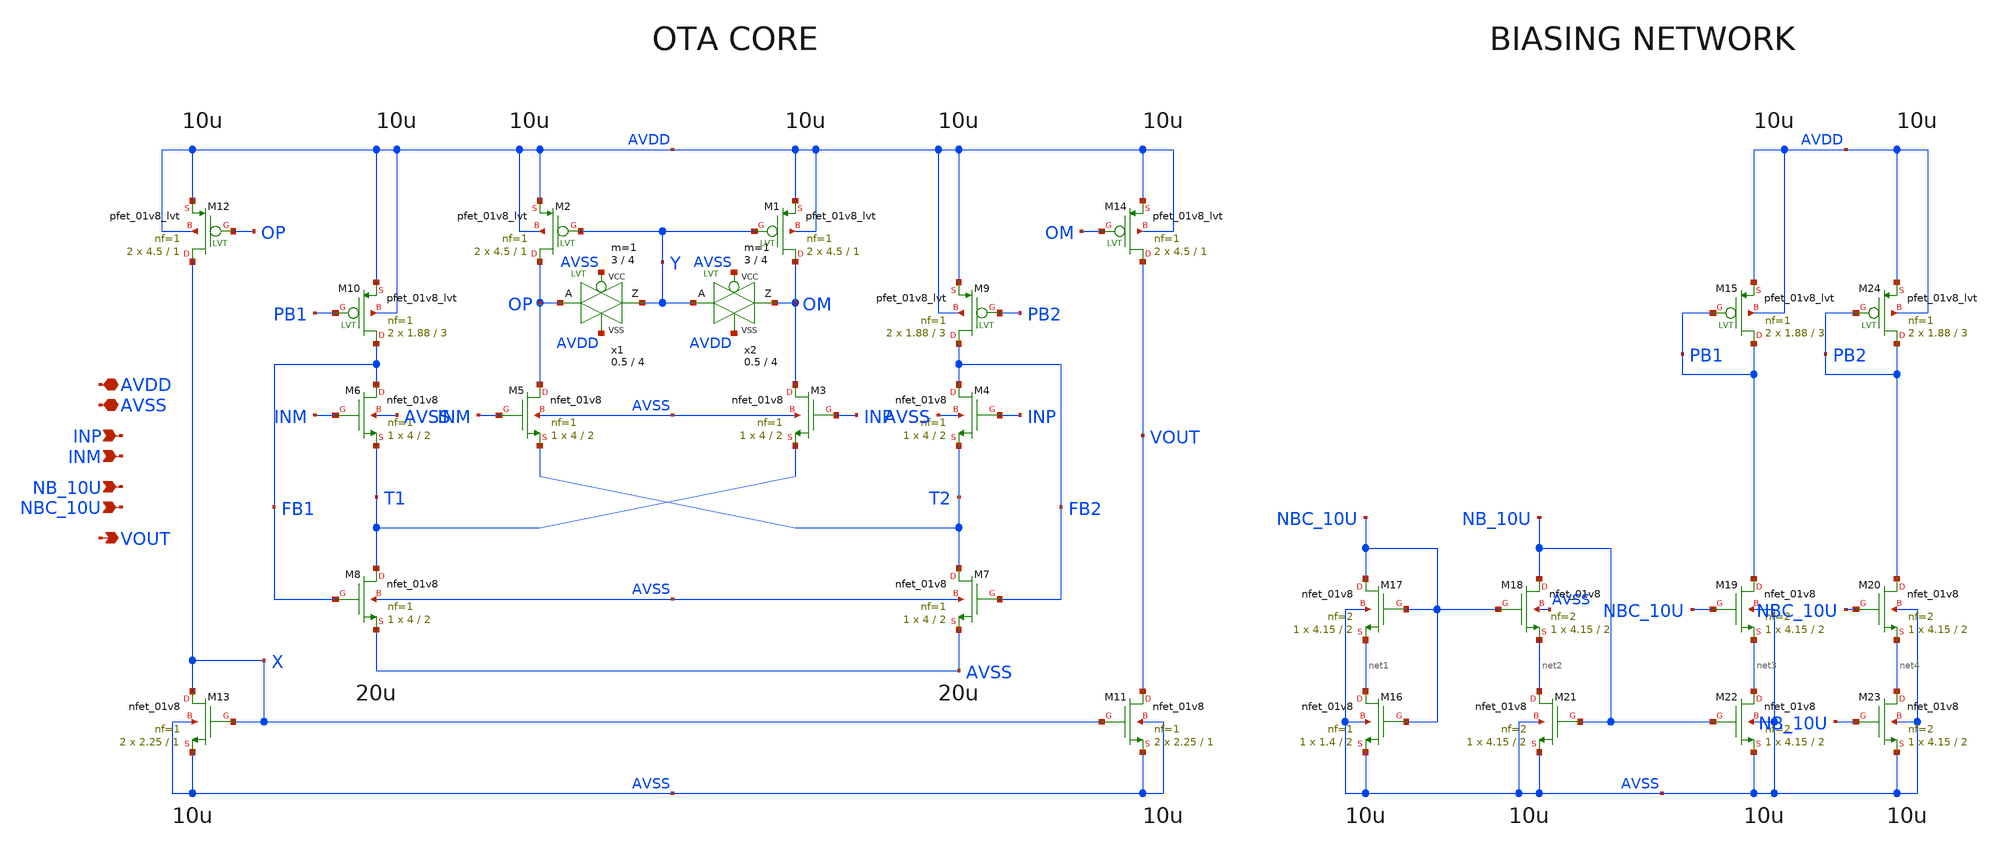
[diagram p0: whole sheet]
** sch_path: ISSCC25/submitted_notebooks/analog_vibes/sim_pex/xschem/ota.sch
**.subckt ota AVDD AVSS INP INM NB_10U NBC_10U VOUT
*.iopin AVDD
*.iopin AVSS
*.ipin INP
*.ipin INM
*.ipin NB_10U
*.ipin NBC_10U
*.opin VOUT
XM1 OM Y AVDD AVDD sky130_fd_pr__pfet_01v8_lvt L=1 W=4.5 nf=1 ad='int((nf+1)/2) * W/nf * 0.29' as='int((nf+2)/2) * W/nf * 0.29'
+ pd='2*int((nf+1)/2) * (W/nf + 0.29)' ps='2*int((nf+2)/2) * (W/nf + 0.29)' nrd='0.29 / W' nrs='0.29 / W'
+ sa=0 sb=0 sd=0 mult=2 m=2
XM2 OP Y AVDD AVDD sky130_fd_pr__pfet_01v8_lvt L=1 W=4.5 nf=1 ad='int((nf+1)/2) * W/nf * 0.29' as='int((nf+2)/2) * W/nf * 0.29'
+ pd='2*int((nf+1)/2) * (W/nf + 0.29)' ps='2*int((nf+2)/2) * (W/nf + 0.29)' nrd='0.29 / W' nrs='0.29 / W'
+ sa=0 sb=0 sd=0 mult=2 m=2
x1 Y OP AVSS AVDD VCC VSS passgate_nlvt W_N=0.5 L_N=4 W_P=3 L_P=4 m=1
x2 OM Y AVSS AVDD VCC VSS passgate_nlvt W_N=0.5 L_N=4 W_P=3 L_P=4 m=1
XM5 OP INM T2 AVSS sky130_fd_pr__nfet_01v8 L=2 W=4 nf=1 ad='int((nf+1)/2) * W/nf * 0.29' as='int((nf+2)/2) * W/nf * 0.29'
+ pd='2*int((nf+1)/2) * (W/nf + 0.29)' ps='2*int((nf+2)/2) * (W/nf + 0.29)' nrd='0.29 / W' nrs='0.29 / W'
+ sa=0 sb=0 sd=0 mult=1 m=1
XM3 OM INP T1 AVSS sky130_fd_pr__nfet_01v8 L=2 W=4 nf=1 ad='int((nf+1)/2) * W/nf * 0.29' as='int((nf+2)/2) * W/nf * 0.29'
+ pd='2*int((nf+1)/2) * (W/nf + 0.29)' ps='2*int((nf+2)/2) * (W/nf + 0.29)' nrd='0.29 / W' nrs='0.29 / W'
+ sa=0 sb=0 sd=0 mult=1 m=1
XM4 FB2 INP T2 AVSS sky130_fd_pr__nfet_01v8 L=2 W=4 nf=1 ad='int((nf+1)/2) * W/nf * 0.29' as='int((nf+2)/2) * W/nf * 0.29'
+ pd='2*int((nf+1)/2) * (W/nf + 0.29)' ps='2*int((nf+2)/2) * (W/nf + 0.29)' nrd='0.29 / W' nrs='0.29 / W'
+ sa=0 sb=0 sd=0 mult=1 m=1
XM6 FB1 INM T1 AVSS sky130_fd_pr__nfet_01v8 L=2 W=4 nf=1 ad='int((nf+1)/2) * W/nf * 0.29' as='int((nf+2)/2) * W/nf * 0.29'
+ pd='2*int((nf+1)/2) * (W/nf + 0.29)' ps='2*int((nf+2)/2) * (W/nf + 0.29)' nrd='0.29 / W' nrs='0.29 / W'
+ sa=0 sb=0 sd=0 mult=1 m=1
XM7 T2 FB2 AVSS AVSS sky130_fd_pr__nfet_01v8 L=2 W=4 nf=1 ad='int((nf+1)/2) * W/nf * 0.29' as='int((nf+2)/2) * W/nf * 0.29'
+ pd='2*int((nf+1)/2) * (W/nf + 0.29)' ps='2*int((nf+2)/2) * (W/nf + 0.29)' nrd='0.29 / W' nrs='0.29 / W'
+ sa=0 sb=0 sd=0 mult=1 m=1
XM8 T1 FB1 AVSS AVSS sky130_fd_pr__nfet_01v8 L=2 W=4 nf=1 ad='int((nf+1)/2) * W/nf * 0.29' as='int((nf+2)/2) * W/nf * 0.29'
+ pd='2*int((nf+1)/2) * (W/nf + 0.29)' ps='2*int((nf+2)/2) * (W/nf + 0.29)' nrd='0.29 / W' nrs='0.29 / W'
+ sa=0 sb=0 sd=0 mult=1 m=1
XM9 FB2 PB2 AVDD AVDD sky130_fd_pr__pfet_01v8_lvt L=3 W=1.88 nf=1 ad='int((nf+1)/2) * W/nf * 0.29' as='int((nf+2)/2) * W/nf * 0.29'
+ pd='2*int((nf+1)/2) * (W/nf + 0.29)' ps='2*int((nf+2)/2) * (W/nf + 0.29)' nrd='0.29 / W' nrs='0.29 / W'
+ sa=0 sb=0 sd=0 mult=2 m=2
XM10 FB1 PB1 AVDD AVDD sky130_fd_pr__pfet_01v8_lvt L=3 W=1.88 nf=1 ad='int((nf+1)/2) * W/nf * 0.29' as='int((nf+2)/2) * W/nf * 0.29'
+ pd='2*int((nf+1)/2) * (W/nf + 0.29)' ps='2*int((nf+2)/2) * (W/nf + 0.29)' nrd='0.29 / W' nrs='0.29 / W'
+ sa=0 sb=0 sd=0 mult=2 m=2
XM14 VOUT OM AVDD AVDD sky130_fd_pr__pfet_01v8_lvt L=1 W=4.5 nf=1 ad='int((nf+1)/2) * W/nf * 0.29' as='int((nf+2)/2) * W/nf * 0.29'
+ pd='2*int((nf+1)/2) * (W/nf + 0.29)' ps='2*int((nf+2)/2) * (W/nf + 0.29)' nrd='0.29 / W' nrs='0.29 / W'
+ sa=0 sb=0 sd=0 mult=2 m=2
XM11 VOUT X AVSS AVSS sky130_fd_pr__nfet_01v8 L=1 W=2.25 nf=1 ad='int((nf+1)/2) * W/nf * 0.29' as='int((nf+2)/2) * W/nf * 0.29'
+ pd='2*int((nf+1)/2) * (W/nf + 0.29)' ps='2*int((nf+2)/2) * (W/nf + 0.29)' nrd='0.29 / W' nrs='0.29 / W'
+ sa=0 sb=0 sd=0 mult=2 m=2
XM12 X OP AVDD AVDD sky130_fd_pr__pfet_01v8_lvt L=1 W=4.5 nf=1 ad='int((nf+1)/2) * W/nf * 0.29' as='int((nf+2)/2) * W/nf * 0.29'
+ pd='2*int((nf+1)/2) * (W/nf + 0.29)' ps='2*int((nf+2)/2) * (W/nf + 0.29)' nrd='0.29 / W' nrs='0.29 / W'
+ sa=0 sb=0 sd=0 mult=2 m=2
XM13 X X AVSS AVSS sky130_fd_pr__nfet_01v8 L=1 W=2.25 nf=1 ad='int((nf+1)/2) * W/nf * 0.29' as='int((nf+2)/2) * W/nf * 0.29'
+ pd='2*int((nf+1)/2) * (W/nf + 0.29)' ps='2*int((nf+2)/2) * (W/nf + 0.29)' nrd='0.29 / W' nrs='0.29 / W'
+ sa=0 sb=0 sd=0 mult=2 m=2
XM16 net1 NBC_10U AVSS AVSS sky130_fd_pr__nfet_01v8 L=2 W=1.4 nf=1 ad='int((nf+1)/2) * W/nf * 0.29' as='int((nf+2)/2) * W/nf * 0.29'
+ pd='2*int((nf+1)/2) * (W/nf + 0.29)' ps='2*int((nf+2)/2) * (W/nf + 0.29)' nrd='0.29 / W' nrs='0.29 / W'
+ sa=0 sb=0 sd=0 mult=1 m=1
XM17 NBC_10U NBC_10U net1 AVSS sky130_fd_pr__nfet_01v8 L=2 W=4.15 nf=2 ad='int((nf+1)/2) * W/nf * 0.29'
+ as='int((nf+2)/2) * W/nf * 0.29' pd='2*int((nf+1)/2) * (W/nf + 0.29)' ps='2*int((nf+2)/2) * (W/nf + 0.29)'
+ nrd='0.29 / W' nrs='0.29 / W' sa=0 sb=0 sd=0 mult=1 m=1
XM18 NB_10U NBC_10U net2 AVSS sky130_fd_pr__nfet_01v8 L=2 W=4.15 nf=2 ad='int((nf+1)/2) * W/nf * 0.29'
+ as='int((nf+2)/2) * W/nf * 0.29' pd='2*int((nf+1)/2) * (W/nf + 0.29)' ps='2*int((nf+2)/2) * (W/nf + 0.29)'
+ nrd='0.29 / W' nrs='0.29 / W' sa=0 sb=0 sd=0 mult=1 m=1
XM19 PB1 NBC_10U net3 AVSS sky130_fd_pr__nfet_01v8 L=2 W=4.15 nf=2 ad='int((nf+1)/2) * W/nf * 0.29' as='int((nf+2)/2) * W/nf * 0.29'
+ pd='2*int((nf+1)/2) * (W/nf + 0.29)' ps='2*int((nf+2)/2) * (W/nf + 0.29)' nrd='0.29 / W' nrs='0.29 / W'
+ sa=0 sb=0 sd=0 mult=1 m=1
XM20 PB2 NBC_10U net4 AVSS sky130_fd_pr__nfet_01v8 L=2 W=4.15 nf=2 ad='int((nf+1)/2) * W/nf * 0.29' as='int((nf+2)/2) * W/nf * 0.29'
+ pd='2*int((nf+1)/2) * (W/nf + 0.29)' ps='2*int((nf+2)/2) * (W/nf + 0.29)' nrd='0.29 / W' nrs='0.29 / W'
+ sa=0 sb=0 sd=0 mult=1 m=1
XM21 net2 NB_10U AVSS AVSS sky130_fd_pr__nfet_01v8 L=2 W=4.15 nf=2 ad='int((nf+1)/2) * W/nf * 0.29' as='int((nf+2)/2) * W/nf * 0.29'
+ pd='2*int((nf+1)/2) * (W/nf + 0.29)' ps='2*int((nf+2)/2) * (W/nf + 0.29)' nrd='0.29 / W' nrs='0.29 / W'
+ sa=0 sb=0 sd=0 mult=1 m=1
XM22 net3 NB_10U AVSS AVSS sky130_fd_pr__nfet_01v8 L=2 W=4.15 nf=2 ad='int((nf+1)/2) * W/nf * 0.29' as='int((nf+2)/2) * W/nf * 0.29'
+ pd='2*int((nf+1)/2) * (W/nf + 0.29)' ps='2*int((nf+2)/2) * (W/nf + 0.29)' nrd='0.29 / W' nrs='0.29 / W'
+ sa=0 sb=0 sd=0 mult=1 m=1
XM23 net4 NB_10U AVSS AVSS sky130_fd_pr__nfet_01v8 L=2 W=4.15 nf=2 ad='int((nf+1)/2) * W/nf * 0.29' as='int((nf+2)/2) * W/nf * 0.29'
+ pd='2*int((nf+1)/2) * (W/nf + 0.29)' ps='2*int((nf+2)/2) * (W/nf + 0.29)' nrd='0.29 / W' nrs='0.29 / W'
+ sa=0 sb=0 sd=0 mult=1 m=1
XM15 PB1 PB1 AVDD AVDD sky130_fd_pr__pfet_01v8_lvt L=3 W=1.88 nf=1 ad='int((nf+1)/2) * W/nf * 0.29' as='int((nf+2)/2) * W/nf * 0.29'
+ pd='2*int((nf+1)/2) * (W/nf + 0.29)' ps='2*int((nf+2)/2) * (W/nf + 0.29)' nrd='0.29 / W' nrs='0.29 / W'
+ sa=0 sb=0 sd=0 mult=2 m=2
XM24 PB2 PB2 AVDD AVDD sky130_fd_pr__pfet_01v8_lvt L=3 W=1.88 nf=1 ad='int((nf+1)/2) * W/nf * 0.29' as='int((nf+2)/2) * W/nf * 0.29'
+ pd='2*int((nf+1)/2) * (W/nf + 0.29)' ps='2*int((nf+2)/2) * (W/nf + 0.29)' nrd='0.29 / W' nrs='0.29 / W'
+ sa=0 sb=0 sd=0 mult=2 m=2
**.ends

* expanding   symbol:  sky130_tests/passgate_nlvt.sym # of pins=4
** sym_path: sky130_tests/passgate_nlvt.sym
** sch_path: sky130_tests/passgate_nlvt.sch
.subckt passgate_nlvt Z A GP GN VCCBPIN VSSBPIN  W_N=1 L_N=0.35 W_P=1 L_P=0.35
*.iopin A
*.iopin Z
*.ipin GP
*.ipin GN
XM1 net1 GN net2 VSS sky130_fd_pr__nfet_01v8_lvt L=L_N W=W_N nf=1 ad=ad as=as pd=pd ps=ps nrd=0
+ nrs=0 sa=0 sb=0 sd=0 mult=1 m=1
XM2 A GP Z VCC sky130_fd_pr__pfet_01v8 W=W_P L=L_P ad=ad pd=pd as=as ps=ps nrd=0 nrs=0 sa=0 sb=0
+ sd=0 nf=1 mult=1
.ends

.end
